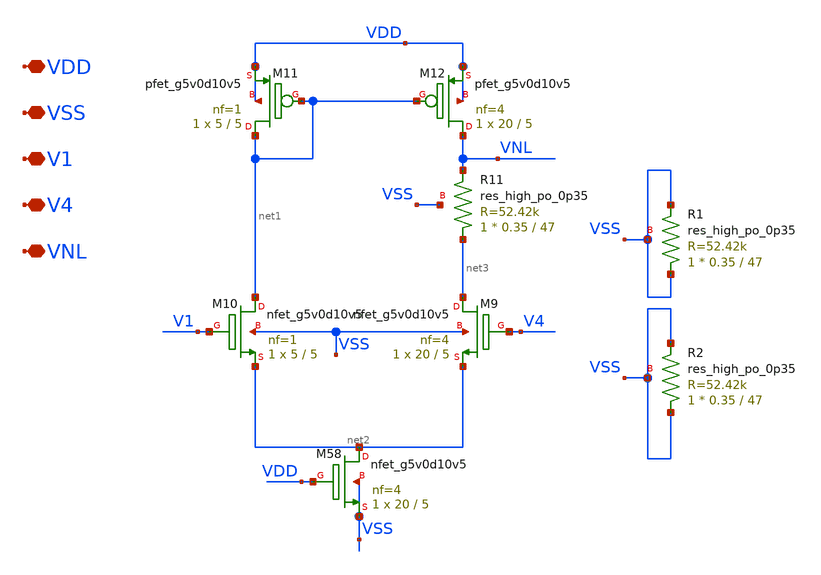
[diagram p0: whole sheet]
** sch_path: xschem/xschem_BGR_Top/BGR_2nd_partb_Mubashir.sch
**.subckt BGR_2nd_partb_Mubashir VDD VSS V1 V4 VNL
*.iopin VDD
*.iopin VSS
*.iopin V1
*.iopin V4
*.iopin VNL
XM9 net3 V4 net2 VSS sky130_fd_pr__nfet_g5v0d10v5 L=5 W=20 nf=4 ad='int((nf+1)/2) * W/nf * 0.29' as='int((nf+2)/2) * W/nf * 0.29'
+ pd='2*int((nf+1)/2) * (W/nf + 0.29)' ps='2*int((nf+2)/2) * (W/nf + 0.29)' nrd='0.29 / W' nrs='0.29 / W'
+ sa=0 sb=0 sd=0 mult=1 m=1
XM10 net1 V1 net2 VSS sky130_fd_pr__nfet_g5v0d10v5 L=5 W=5 nf=1 ad='int((nf+1)/2) * W/nf * 0.29' as='int((nf+2)/2) * W/nf * 0.29'
+ pd='2*int((nf+1)/2) * (W/nf + 0.29)' ps='2*int((nf+2)/2) * (W/nf + 0.29)' nrd='0.29 / W' nrs='0.29 / W'
+ sa=0 sb=0 sd=0 mult=1 m=1
XM11 net1 net1 VDD VDD sky130_fd_pr__pfet_g5v0d10v5 L=5 W=5 nf=1 ad='int((nf+1)/2) * W/nf * 0.29' as='int((nf+2)/2) * W/nf * 0.29'
+ pd='2*int((nf+1)/2) * (W/nf + 0.29)' ps='2*int((nf+2)/2) * (W/nf + 0.29)' nrd='0.29 / W' nrs='0.29 / W'
+ sa=0 sb=0 sd=0 mult=1 m=1
XM12 VNL net1 VDD VDD sky130_fd_pr__pfet_g5v0d10v5 L=5 W=20 nf=4 ad='int((nf+1)/2) * W/nf * 0.29' as='int((nf+2)/2) * W/nf * 0.29'
+ pd='2*int((nf+1)/2) * (W/nf + 0.29)' ps='2*int((nf+2)/2) * (W/nf + 0.29)' nrd='0.29 / W' nrs='0.29 / W'
+ sa=0 sb=0 sd=0 mult=1 m=1
XM58 net2 VDD VSS VSS sky130_fd_pr__nfet_g5v0d10v5 L=5 W=20 nf=4 ad='int((nf+1)/2) * W/nf * 0.29' as='int((nf+2)/2) * W/nf * 0.29'
+ pd='2*int((nf+1)/2) * (W/nf + 0.29)' ps='2*int((nf+2)/2) * (W/nf + 0.29)' nrd='0.29 / W' nrs='0.29 / W'
+ sa=0 sb=0 sd=0 mult=1 m=1
XR11 net3 VNL VSS sky130_fd_pr__res_high_po_0p35 L=47 mult=1 m=1
XR1 VSS VSS VSS sky130_fd_pr__res_high_po_0p35 L=47 mult=1 m=1
XR2 VSS VSS VSS sky130_fd_pr__res_high_po_0p35 L=47 mult=1 m=1
**.ends
.end
